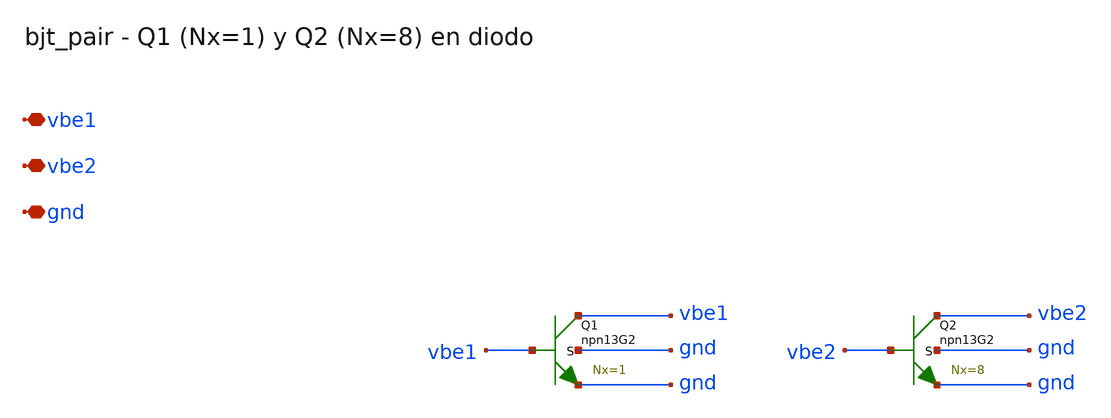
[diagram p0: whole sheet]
** sch_path: Enfoque_A/xschem/celdas/bjt_pair.sch
**.subckt bjt_pair vbe1 vbe2 gnd
*.iopin vbe1
*.iopin vbe2
*.iopin gnd
XQ1 vbe1 vbe1 gnd gnd npn13G2 Nx=1 mm_ok=1
XQ2 vbe2 vbe2 gnd gnd npn13G2 Nx=8 mm_ok=1
**.ends
.end
